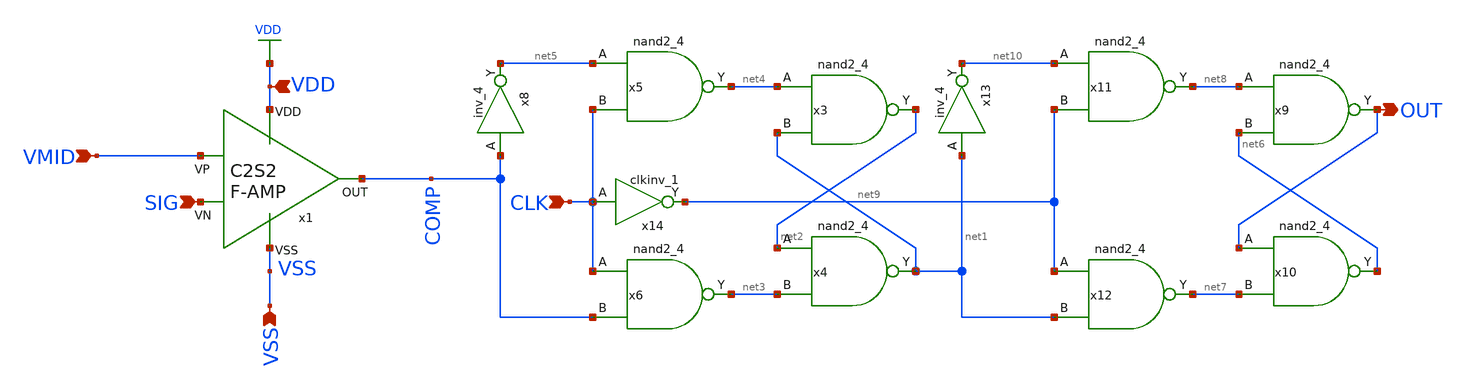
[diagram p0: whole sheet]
** sch_path: DeltaSigma/xschem/1Bit_Clk_ADC.sch
.lib $::SKYWATER_MODELS/sky130.lib.spice tt
.include $::SKYWATER_STDCELLS/sky130_fd_sc_hd.spice

**.subckt 1Bit_Clk_ADC SIG VDD VSS CLK OUT VMID
*.ipin SIG
*.ipin VDD
*.ipin VSS
*.ipin CLK
*.opin OUT
*.ipin VMID
x3 net4 net1 VSS VSS VDD VDD net2 sky130_fd_sc_hd__nand2_4
x4 net2 net3 VSS VSS VDD VDD net1 sky130_fd_sc_hd__nand2_4
x5 net5 CLK VSS VSS VDD VDD net4 sky130_fd_sc_hd__nand2_4
x6 CLK COMP VSS VSS VDD VDD net3 sky130_fd_sc_hd__nand2_4
x8 COMP VSS VSS VDD VDD net5 sky130_fd_sc_hd__inv_4
x9 net8 net6 VSS VSS VDD VDD OUT sky130_fd_sc_hd__nand2_4
x10 OUT net7 VSS VSS VDD VDD net6 sky130_fd_sc_hd__nand2_4
x11 net10 net9 VSS VSS VDD VDD net8 sky130_fd_sc_hd__nand2_4
x12 net9 net1 VSS VSS VDD VDD net7 sky130_fd_sc_hd__nand2_4
x14 CLK VSS VSS VDD VDD net9 sky130_fd_sc_hd__clkinv_1
x13 net1 VSS VSS VDD VDD net10 sky130_fd_sc_hd__inv_4
x1 VDD VMID SIG COMP VSS C2S2_Amp_F
**.ends
.GLOBAL VDD
.end
